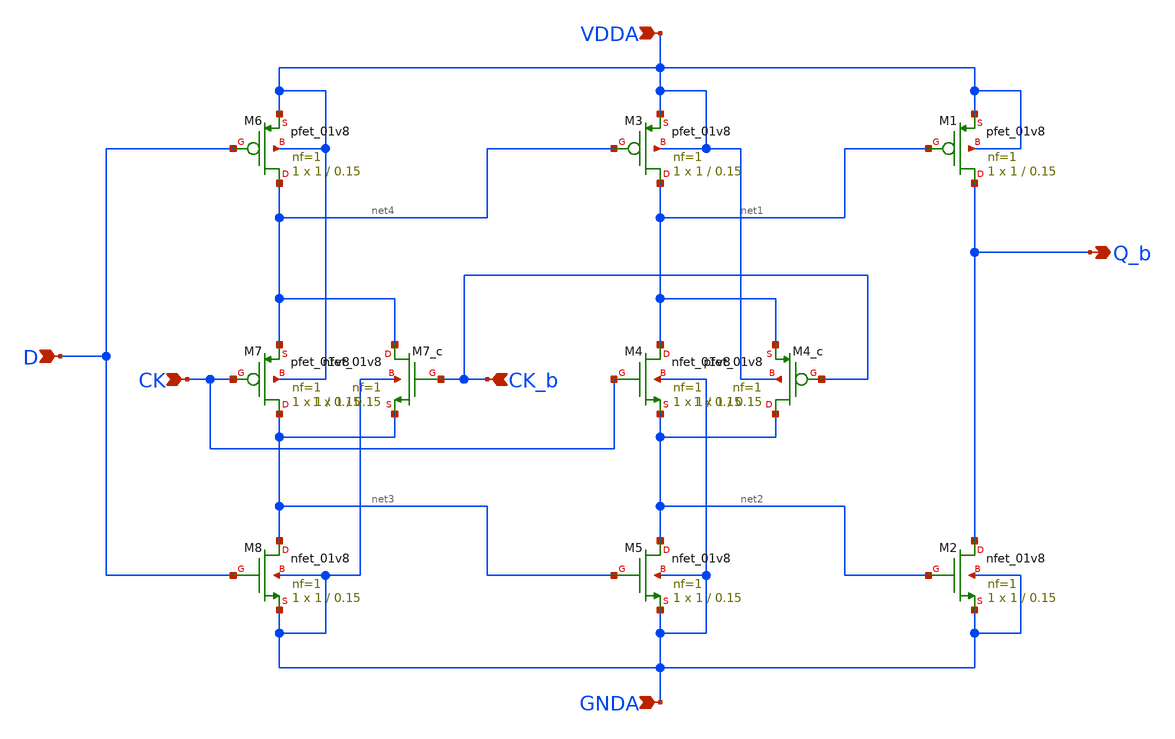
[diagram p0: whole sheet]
** sch_path: projects/pll/divider/xschem_ngspice/TSPC_FF_comp_sw.sch
**.subckt TSPC_FF_comp_sw CK D Q_b VDDA GNDA CK_b
*.ipin CK
*.ipin D
*.opin Q_b
*.ipin VDDA
*.ipin GNDA
*.ipin CK_b
XM1 Q_b net1 VDDA VDDA sky130_fd_pr__pfet_01v8 L=0.15 W=1 nf=1 ad='int((nf+1)/2) * W/nf * 0.29' as='int((nf+2)/2) * W/nf * 0.29'
+ pd='2*int((nf+1)/2) * (W/nf + 0.29)' ps='2*int((nf+2)/2) * (W/nf + 0.29)' nrd='0.29 / W' nrs='0.29 / W'
+ sa=0 sb=0 sd=0 mult=1 m=1
XM4 net1 CK net2 GNDA sky130_fd_pr__nfet_01v8 L=0.15 W=1 nf=1 ad='int((nf+1)/2) * W/nf * 0.29' as='int((nf+2)/2) * W/nf * 0.29'
+ pd='2*int((nf+1)/2) * (W/nf + 0.29)' ps='2*int((nf+2)/2) * (W/nf + 0.29)' nrd='0.29 / W' nrs='0.29 / W'
+ sa=0 sb=0 sd=0 mult=1 m=1
XM2 Q_b net2 GNDA GNDA sky130_fd_pr__nfet_01v8 L=0.15 W=1 nf=1 ad='int((nf+1)/2) * W/nf * 0.29' as='int((nf+2)/2) * W/nf * 0.29'
+ pd='2*int((nf+1)/2) * (W/nf + 0.29)' ps='2*int((nf+2)/2) * (W/nf + 0.29)' nrd='0.29 / W' nrs='0.29 / W'
+ sa=0 sb=0 sd=0 mult=1 m=1
XM3 net1 net4 VDDA VDDA sky130_fd_pr__pfet_01v8 L=0.15 W=1 nf=1 ad='int((nf+1)/2) * W/nf * 0.29' as='int((nf+2)/2) * W/nf * 0.29'
+ pd='2*int((nf+1)/2) * (W/nf + 0.29)' ps='2*int((nf+2)/2) * (W/nf + 0.29)' nrd='0.29 / W' nrs='0.29 / W'
+ sa=0 sb=0 sd=0 mult=1 m=1
XM5 net2 net3 GNDA GNDA sky130_fd_pr__nfet_01v8 L=0.15 W=1 nf=1 ad='int((nf+1)/2) * W/nf * 0.29' as='int((nf+2)/2) * W/nf * 0.29'
+ pd='2*int((nf+1)/2) * (W/nf + 0.29)' ps='2*int((nf+2)/2) * (W/nf + 0.29)' nrd='0.29 / W' nrs='0.29 / W'
+ sa=0 sb=0 sd=0 mult=1 m=1
XM6 net4 D VDDA VDDA sky130_fd_pr__pfet_01v8 L=0.15 W=1 nf=1 ad='int((nf+1)/2) * W/nf * 0.29' as='int((nf+2)/2) * W/nf * 0.29'
+ pd='2*int((nf+1)/2) * (W/nf + 0.29)' ps='2*int((nf+2)/2) * (W/nf + 0.29)' nrd='0.29 / W' nrs='0.29 / W'
+ sa=0 sb=0 sd=0 mult=1 m=1
XM8 net3 D GNDA GNDA sky130_fd_pr__nfet_01v8 L=0.15 W=1 nf=1 ad='int((nf+1)/2) * W/nf * 0.29' as='int((nf+2)/2) * W/nf * 0.29'
+ pd='2*int((nf+1)/2) * (W/nf + 0.29)' ps='2*int((nf+2)/2) * (W/nf + 0.29)' nrd='0.29 / W' nrs='0.29 / W'
+ sa=0 sb=0 sd=0 mult=1 m=1
XM7 net3 CK net4 VDDA sky130_fd_pr__pfet_01v8 L=0.15 W=1 nf=1 ad='int((nf+1)/2) * W/nf * 0.29' as='int((nf+2)/2) * W/nf * 0.29'
+ pd='2*int((nf+1)/2) * (W/nf + 0.29)' ps='2*int((nf+2)/2) * (W/nf + 0.29)' nrd='0.29 / W' nrs='0.29 / W'
+ sa=0 sb=0 sd=0 mult=1 m=1
XM4_c net2 CK_b net1 VDDA sky130_fd_pr__pfet_01v8 L=0.15 W=1 nf=1 ad='int((nf+1)/2) * W/nf * 0.29' as='int((nf+2)/2) * W/nf * 0.29'
+ pd='2*int((nf+1)/2) * (W/nf + 0.29)' ps='2*int((nf+2)/2) * (W/nf + 0.29)' nrd='0.29 / W' nrs='0.29 / W'
+ sa=0 sb=0 sd=0 mult=1 m=1
XM7_c net4 CK_b net3 GNDA sky130_fd_pr__nfet_01v8 L=0.15 W=1 nf=1 ad='int((nf+1)/2) * W/nf * 0.29' as='int((nf+2)/2) * W/nf * 0.29'
+ pd='2*int((nf+1)/2) * (W/nf + 0.29)' ps='2*int((nf+2)/2) * (W/nf + 0.29)' nrd='0.29 / W' nrs='0.29 / W'
+ sa=0 sb=0 sd=0 mult=1 m=1
**.ends
.end
